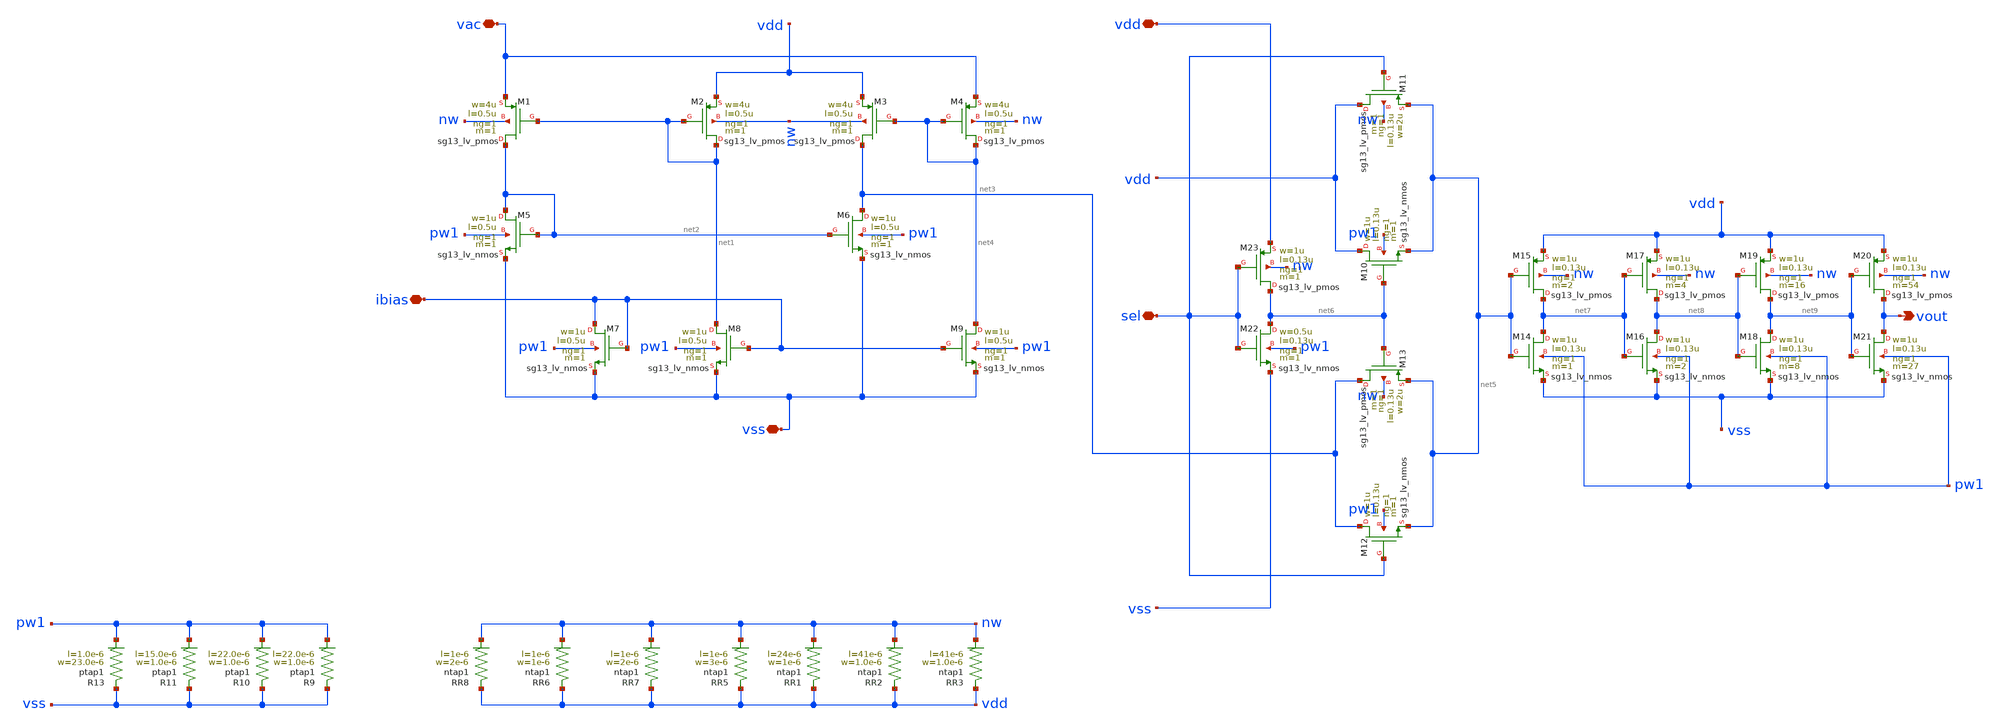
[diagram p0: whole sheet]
** sch_path: Layouts/driver/driver_v2.sch
**.subckt driver_v2 vdd vout ibias vac vss sel
*.iopin vdd
*.opin vout
*.iopin ibias
*.iopin vac
*.iopin vss
*.iopin sel
XM1 net2 net1 vac nw sg13_lv_pmos w=4u l=0.5u ng=1 m=1 mm_ok=1
XM2 net1 net1 vdd nw sg13_lv_pmos w=4u l=0.5u ng=1 m=1 mm_ok=1
XM3 net3 net4 vdd nw sg13_lv_pmos w=4u l=0.5u ng=1 m=1 mm_ok=1
XM4 net4 net4 vac nw sg13_lv_pmos w=4u l=0.5u ng=1 m=1 mm_ok=1
XM5 net2 net2 vss pw1 sg13_lv_nmos w=1u l=0.5u ng=1 m=1 mm_ok=1
XM6 net3 net2 vss pw1 sg13_lv_nmos w=1u l=0.5u ng=1 m=1 mm_ok=1
XM8 net1 ibias vss pw1 sg13_lv_nmos w=1u l=0.5u ng=1 m=1 mm_ok=1
XM7 ibias ibias vss pw1 sg13_lv_nmos w=1u l=0.5u ng=1 m=1 mm_ok=1
XM9 net4 ibias vss pw1 sg13_lv_nmos w=1u l=0.5u ng=1 m=1 mm_ok=1
XR1 vdd nw ntap1 R=13.24 w=1e-6 l=24e-6
XR2 vdd nw ntap1 R=7.84 w=1.0e-6 l=41e-6
XR3 vdd nw ntap1 R=7.84 w=1.0e-6 l=41e-6
XM10 vdd net6 net5 pw1 sg13_lv_nmos w=1u l=0.13u ng=1 m=1 mm_ok=1
XM11 vdd sel net5 nw sg13_lv_pmos w=2u l=0.13u ng=1 m=1 mm_ok=1
XM12 net3 sel net5 pw1 sg13_lv_nmos w=1u l=0.13u ng=1 m=1 mm_ok=1
XM13 net3 net6 net5 nw sg13_lv_pmos w=2u l=0.13u ng=1 m=1 mm_ok=1
XM14 net7 net5 vss pw1 sg13_lv_nmos w=1u l=0.13u ng=1 m=1 mm_ok=1
XM15 net7 net5 vdd nw sg13_lv_pmos w=1u l=0.13u ng=1 m=2 mm_ok=1
XM16 net8 net7 vss pw1 sg13_lv_nmos w=1u l=0.13u ng=1 m=2 mm_ok=1
XM17 net8 net7 vdd nw sg13_lv_pmos w=1u l=0.13u ng=1 m=4 mm_ok=1
XM18 net9 net8 vss pw1 sg13_lv_nmos w=1u l=0.13u ng=1 m=8 mm_ok=1
XM19 net9 net8 vdd nw sg13_lv_pmos w=1u l=0.13u ng=1 m=16 mm_ok=1
XM20 vout net9 vdd nw sg13_lv_pmos w=1u l=0.13u ng=1 m=54 mm_ok=1
XM21 vout net9 vss pw1 sg13_lv_nmos w=1u l=0.13u ng=1 m=27 mm_ok=1
XR5 vdd nw ntap1 R=89.09 w=3e-6 l=1e-6
XR6 vdd nw ntap1 R=196 w=1e-6 l=1e-6
XR7 vdd nw ntap1 R=122.5 w=2e-6 l=1e-6
XR8 vdd nw ntap1 R=122.5 w=2e-6 l=1e-6
XR13 vss pw1 ptap1 R=13.8 w=23.0e-6 l=1.0e-6
XR11 vss pw1 ptap1 R=20.85 w=1.0e-6 l=15.0e-6
XR10 vss pw1 ptap1 R=14.41 w=1.0e-6 l=22.0e-6
XR9 vss pw1 ptap1 R=14.41 w=1.0e-6 l=22.0e-6
XM22 net6 sel vss pw1 sg13_lv_nmos w=0.5u l=0.13u ng=1 m=1 mm_ok=1
XM23 net6 sel vdd nw sg13_lv_pmos w=1u l=0.13u ng=1 m=1 mm_ok=1
**.ends
.end
